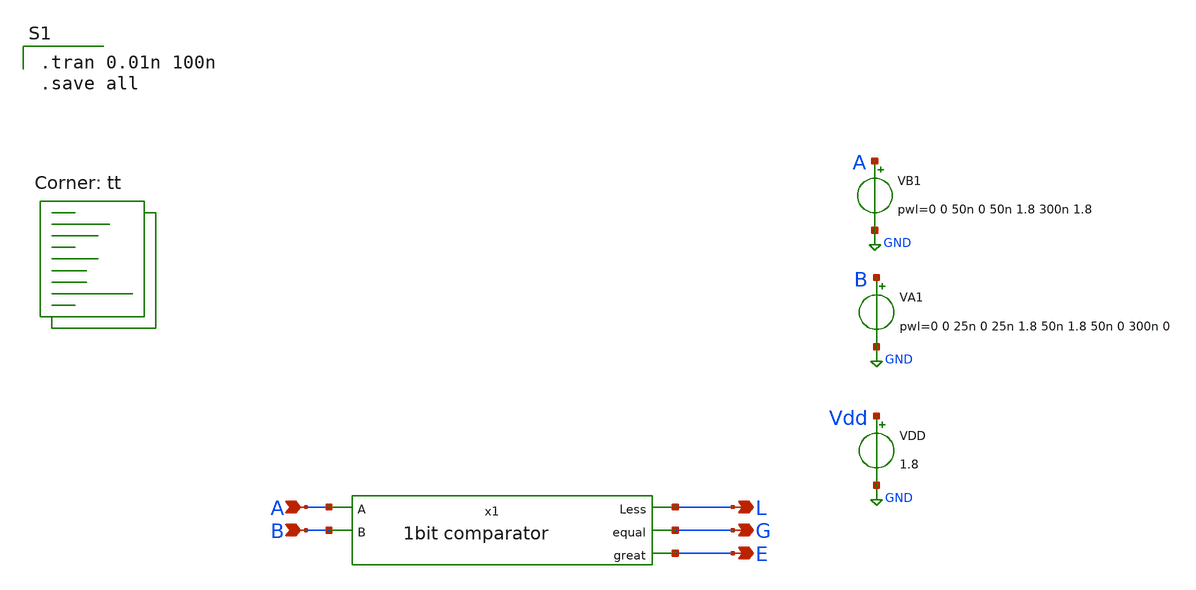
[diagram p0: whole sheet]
** sch_path: gates/1bit comparatorsymsim.sch
**.subckt 1bit comparatorsymsim L G E A B
*.opin L
*.opin G
*.opin E
*.ipin A
*.ipin B
x1 L A G B E 1bit comparator
VDD Vdd GND 1.8
VA1 B GND pwl=0 0 25n 0 25n 1.8 50n 1.8 50n 0 300n 0
VB1 A GND pwl=0 0 50n 0 50n 1.8 300n 1.8
**** begin user architecture code

.tran 0.01n 100n
.save all

.lib $::SKYWATER_MODELS/sky130.lib.spice tt
**** end user architecture code
**.ends

* expanding   symbol:  1bit comparator.sym # of pins=5
** sym_path: gates/1bit comparator.sym
** sch_path: gates/1bit comparator.sch
.subckt 1bit comparator Less A equal B great
*.ipin A
*.ipin B
*.opin Less
*.opin equal
*.opin great
X1 A net1 inv_vtc
X2 B net2 inv_vtc
x3 net1 Less B AND2
x4 A great net2 AND2
x5 Less equal great NOR2
.ends


* expanding   symbol:  /home/apn/test_xschem_sky130/inv_vtc.sym # of pins=2
** sym_path: gates/inv_vtc.sym
** sch_path: gates/inv_vtc.sch
.subckt inv_vtc A Y
*.ipin A
*.opin Y
XM1 Y A VDD VDD sky130_fd_pr__pfet_01v8 L=0.15 W=2 nf=1 ad='int((nf+1)/2) * W/nf * 0.29' as='int((nf+2)/2) * W/nf * 0.29'
+ pd='2*int((nf+1)/2) * (W/nf + 0.29)' ps='2*int((nf+2)/2) * (W/nf + 0.29)' nrd='0.29 / W' nrs='0.29 / W'
+ sa=0 sb=0 sd=0 mult=1 m=1
XM2 Y A GND GND sky130_fd_pr__nfet_01v8 L=0.15 W=1 nf=1 ad='int((nf+1)/2) * W/nf * 0.29' as='int((nf+2)/2) * W/nf * 0.29'
+ pd='2*int((nf+1)/2) * (W/nf + 0.29)' ps='2*int((nf+2)/2) * (W/nf + 0.29)' nrd='0.29 / W' nrs='0.29 / W'
+ sa=0 sb=0 sd=0 mult=1 m=1
.ends


* expanding   symbol:  AND2.sym # of pins=3
** sym_path: gates/AND2.sym
** sch_path: gates/AND2.sch
.subckt AND2 A Y B
*.opin Y
*.ipin A
*.ipin B
x1 A net1 B NAND2_Gate
X2 net1 Y inv_vtc
.ends


* expanding   symbol:  NOR2.sym # of pins=3
** sym_path: gates/NOR2.sym
** sch_path: gates/NOR2.sch
.subckt NOR2 B Y A
*.ipin A
*.ipin B
*.opin Y
XM7 VDD B net1 VDD sky130_fd_pr__pfet_01v8 L=0.15 W=1 nf=1 ad='int((nf+1)/2) * W/nf * 0.29' as='int((nf+2)/2) * W/nf * 0.29'
+ pd='2*int((nf+1)/2) * (W/nf + 0.29)' ps='2*int((nf+2)/2) * (W/nf + 0.29)' nrd='0.29 / W' nrs='0.29 / W'
+ sa=0 sb=0 sd=0 mult=1 m=1
XM8 GND B Y GND sky130_fd_pr__nfet_01v8 L=0.15 W=1 nf=1 ad='int((nf+1)/2) * W/nf * 0.29' as='int((nf+2)/2) * W/nf * 0.29'
+ pd='2*int((nf+1)/2) * (W/nf + 0.29)' ps='2*int((nf+2)/2) * (W/nf + 0.29)' nrd='0.29 / W' nrs='0.29 / W'
+ sa=0 sb=0 sd=0 mult=1 m=1
XM9 net1 A Y VDD sky130_fd_pr__pfet_01v8 L=0.15 W=1 nf=1 ad='int((nf+1)/2) * W/nf * 0.29' as='int((nf+2)/2) * W/nf * 0.29'
+ pd='2*int((nf+1)/2) * (W/nf + 0.29)' ps='2*int((nf+2)/2) * (W/nf + 0.29)' nrd='0.29 / W' nrs='0.29 / W'
+ sa=0 sb=0 sd=0 mult=1 m=1
XM10 GND A Y GND sky130_fd_pr__nfet_01v8 L=0.15 W=1 nf=1 ad='int((nf+1)/2) * W/nf * 0.29' as='int((nf+2)/2) * W/nf * 0.29'
+ pd='2*int((nf+1)/2) * (W/nf + 0.29)' ps='2*int((nf+2)/2) * (W/nf + 0.29)' nrd='0.29 / W' nrs='0.29 / W'
+ sa=0 sb=0 sd=0 mult=1 m=1
.ends


* expanding   symbol:  NAND2_Gate.sym # of pins=3
** sym_path: gates/NAND2_Gate.sym
** sch_path: gates/NAND2_Gate.sch
.subckt NAND2_Gate A Y B
*.ipin A
*.ipin B
*.opin Y
XM1 Y A net1 GND sky130_fd_pr__nfet_01v8 L=0.15 W=1 nf=1 ad='int((nf+1)/2) * W/nf * 0.29' as='int((nf+2)/2) * W/nf * 0.29'
+ pd='2*int((nf+1)/2) * (W/nf + 0.29)' ps='2*int((nf+2)/2) * (W/nf + 0.29)' nrd='0.29 / W' nrs='0.29 / W'
+ sa=0 sb=0 sd=0 mult=1 m=1
XM2 net1 B GND GND sky130_fd_pr__nfet_01v8 L=0.15 W=1 nf=1 ad='int((nf+1)/2) * W/nf * 0.29' as='int((nf+2)/2) * W/nf * 0.29'
+ pd='2*int((nf+1)/2) * (W/nf + 0.29)' ps='2*int((nf+2)/2) * (W/nf + 0.29)' nrd='0.29 / W' nrs='0.29 / W'
+ sa=0 sb=0 sd=0 mult=1 m=1
XM3 Y A VDD VDD sky130_fd_pr__pfet_01v8 L=0.15 W=1 nf=1 ad='int((nf+1)/2) * W/nf * 0.29' as='int((nf+2)/2) * W/nf * 0.29'
+ pd='2*int((nf+1)/2) * (W/nf + 0.29)' ps='2*int((nf+2)/2) * (W/nf + 0.29)' nrd='0.29 / W' nrs='0.29 / W'
+ sa=0 sb=0 sd=0 mult=1 m=1
XM4 Y B VDD VDD sky130_fd_pr__pfet_01v8 L=0.15 W=1 nf=1 ad='int((nf+1)/2) * W/nf * 0.29' as='int((nf+2)/2) * W/nf * 0.29'
+ pd='2*int((nf+1)/2) * (W/nf + 0.29)' ps='2*int((nf+2)/2) * (W/nf + 0.29)' nrd='0.29 / W' nrs='0.29 / W'
+ sa=0 sb=0 sd=0 mult=1 m=1
.ends

.GLOBAL GND
.GLOBAL VDD
.end
